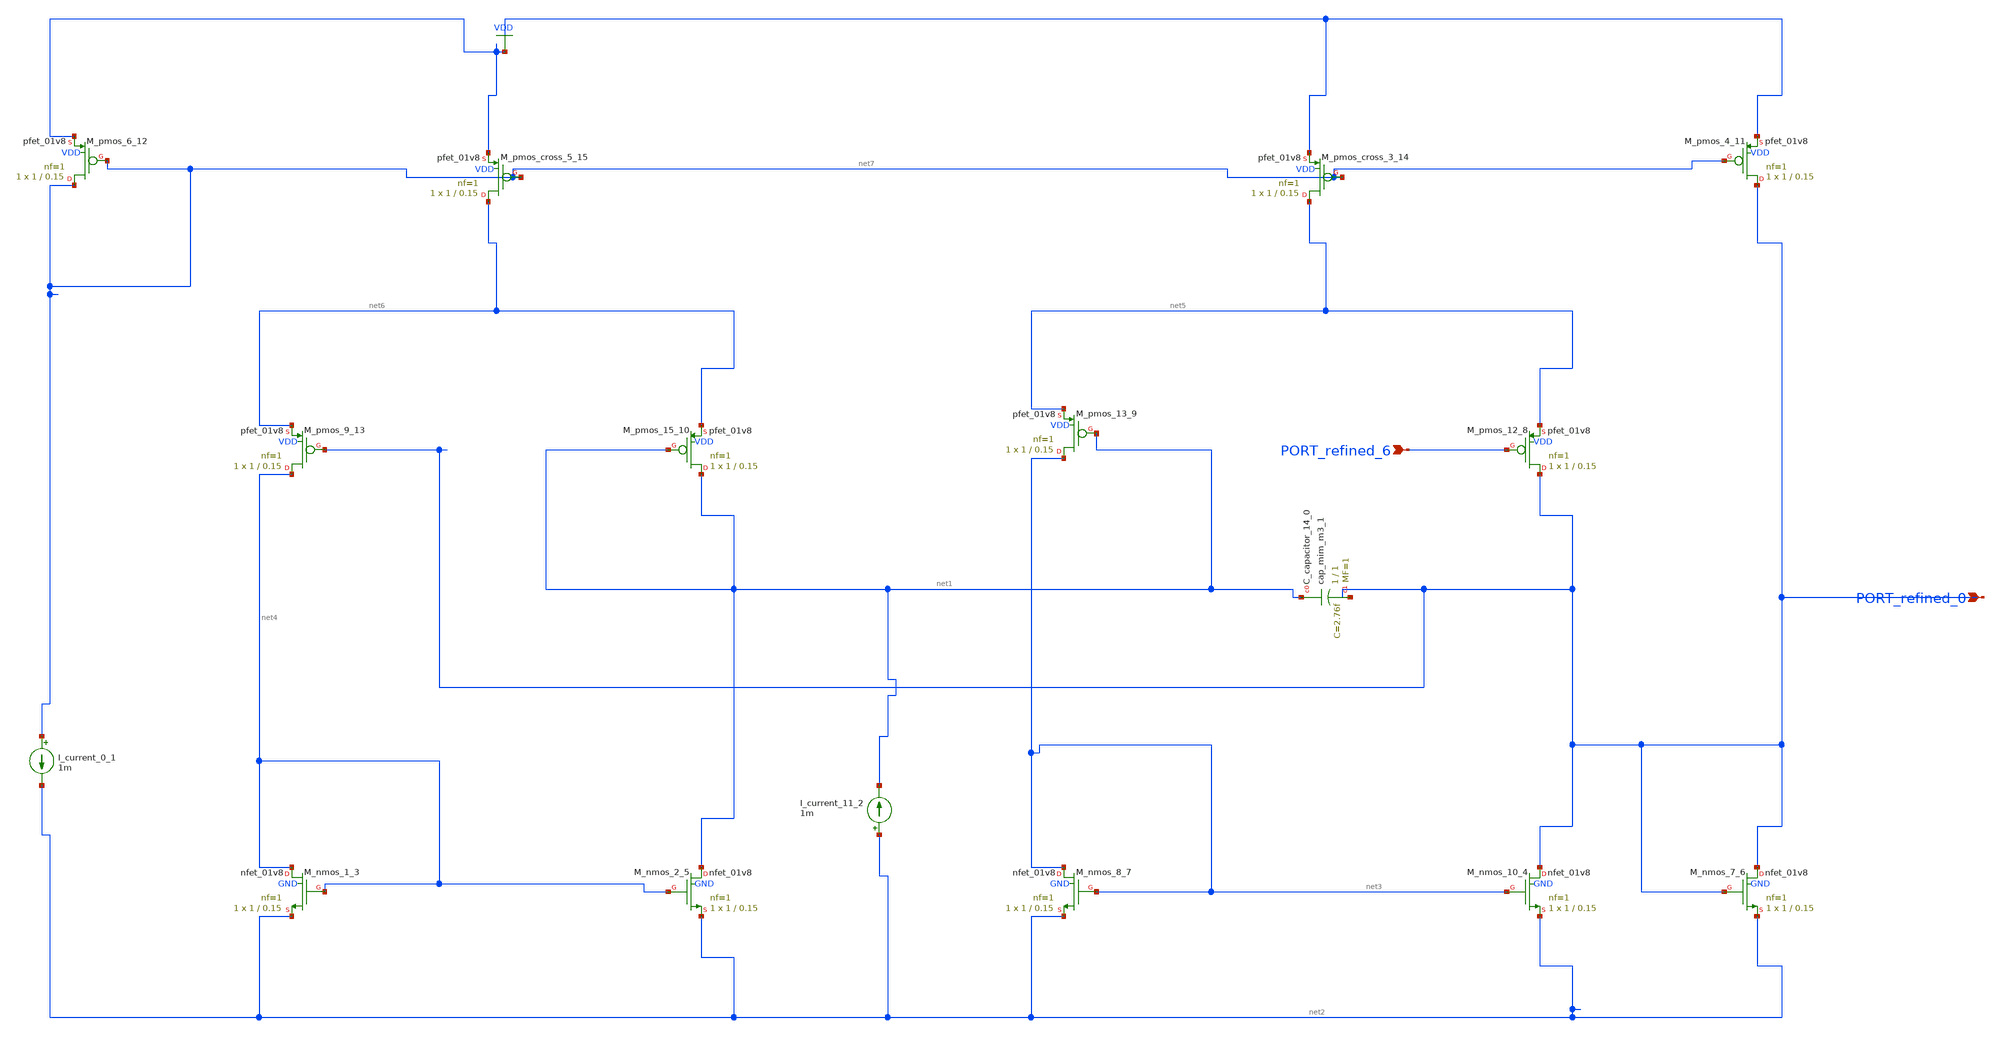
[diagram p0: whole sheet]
** sch_path: schematics/10_1016_j_vlsi_2023_02_005_06_002.sch
**.subckt 10_1016_j_vlsi_2023_02_005_06_002 PORT_refined_0 PORT_refined_6
*.ipin PORT_refined_0
*.ipin PORT_refined_6
XC_capacitor_14_0 net1 PORT_refined_0 sky130_fd_pr__cap_mim_m3_1 W=1 L=1 MF=1 m=1
I_current_0_1 net7 net2 1m
I_current_11_2 net2 net1 1m
XM_nmos_1_3 net4 net4 net2 GND sky130_fd_pr__nfet_01v8 L=0.15 W=1 nf=1 ad='int((1 + 1)/2) * 1 / 1 * 0.29'
+ as='int((1 + 2)/2) * 1 / 1 * 0.29' pd='2*int((1 + 1)/2) * (1 / 1 + 0.29)' ps='2*int((1 + 2)/2) * (1 / 1 + 0.29)'
+ nrd='0.29 / 1 ' nrs='0.29 / 1 ' sa=0 sb=0 sd=0 mult=1 m=1
XM_nmos_10_4 PORT_refined_0 net3 net2 GND sky130_fd_pr__nfet_01v8 L=0.15 W=1 nf=1 ad='int((1 + 1)/2) * 1 / 1 * 0.29'
+ as='int((1 + 2)/2) * 1 / 1 * 0.29' pd='2*int((1 + 1)/2) * (1 / 1 + 0.29)' ps='2*int((1 + 2)/2) * (1 / 1 + 0.29)'
+ nrd='0.29 / 1 ' nrs='0.29 / 1 ' sa=0 sb=0 sd=0 mult=1 m=1
XM_nmos_2_5 net1 net4 net2 GND sky130_fd_pr__nfet_01v8 L=0.15 W=1 nf=1 ad='int((1 + 1)/2) * 1 / 1 * 0.29'
+ as='int((1 + 2)/2) * 1 / 1 * 0.29' pd='2*int((1 + 1)/2) * (1 / 1 + 0.29)' ps='2*int((1 + 2)/2) * (1 / 1 + 0.29)'
+ nrd='0.29 / 1 ' nrs='0.29 / 1 ' sa=0 sb=0 sd=0 mult=1 m=1
XM_nmos_7_6 PORT_refined_0 PORT_refined_0 net2 GND sky130_fd_pr__nfet_01v8 L=0.15 W=1 nf=1 ad='int((1 + 1)/2) * 1 / 1 * 0.29'
+ as='int((1 + 2)/2) * 1 / 1 * 0.29' pd='2*int((1 + 1)/2) * (1 / 1 + 0.29)' ps='2*int((1 + 2)/2) * (1 / 1 + 0.29)'
+ nrd='0.29 / 1 ' nrs='0.29 / 1 ' sa=0 sb=0 sd=0 mult=1 m=1
XM_nmos_8_7 net3 net3 net2 GND sky130_fd_pr__nfet_01v8 L=0.15 W=1 nf=1 ad='int((1 + 1)/2) * 1 / 1 * 0.29'
+ as='int((1 + 2)/2) * 1 / 1 * 0.29' pd='2*int((1 + 1)/2) * (1 / 1 + 0.29)' ps='2*int((1 + 2)/2) * (1 / 1 + 0.29)'
+ nrd='0.29 / 1 ' nrs='0.29 / 1 ' sa=0 sb=0 sd=0 mult=1 m=1
XM_pmos_12_8 PORT_refined_0 PORT_refined_6 net5 VDD sky130_fd_pr__pfet_01v8 L=0.15 W=1 nf=1 ad='int((1 + 1)/2) * 1 / 1 * 0.29'
+ as='int((1 + 2)/2) * 1 / 1 * 0.29' pd='2*int((1 + 1)/2) * (1 / 1 + 0.29)' ps='2*int((1 + 2)/2) * (1 / 1 + 0.29)'
+ nrd='0.29 / 1 ' nrs='0.29 / 1 ' sa=0 sb=0 sd=0 mult=1 m=1
XM_pmos_13_9 net3 net1 net5 VDD sky130_fd_pr__pfet_01v8 L=0.15 W=1 nf=1 ad='int((1 + 1)/2) * 1 / 1 * 0.29'
+ as='int((1 + 2)/2) * 1 / 1 * 0.29' pd='2*int((1 + 1)/2) * (1 / 1 + 0.29)' ps='2*int((1 + 2)/2) * (1 / 1 + 0.29)'
+ nrd='0.29 / 1 ' nrs='0.29 / 1 ' sa=0 sb=0 sd=0 mult=1 m=1
XM_pmos_15_10 net1 net1 net6 VDD sky130_fd_pr__pfet_01v8 L=0.15 W=1 nf=1 ad='int((1 + 1)/2) * 1 / 1 * 0.29'
+ as='int((1 + 2)/2) * 1 / 1 * 0.29' pd='2*int((1 + 1)/2) * (1 / 1 + 0.29)' ps='2*int((1 + 2)/2) * (1 / 1 + 0.29)'
+ nrd='0.29 / 1 ' nrs='0.29 / 1 ' sa=0 sb=0 sd=0 mult=1 m=1
XM_pmos_4_11 PORT_refined_0 net7 VDD VDD sky130_fd_pr__pfet_01v8 L=0.15 W=1 nf=1 ad='int((1 + 1)/2) * 1 / 1 * 0.29'
+ as='int((1 + 2)/2) * 1 / 1 * 0.29' pd='2*int((1 + 1)/2) * (1 / 1 + 0.29)' ps='2*int((1 + 2)/2) * (1 / 1 + 0.29)'
+ nrd='0.29 / 1 ' nrs='0.29 / 1 ' sa=0 sb=0 sd=0 mult=1 m=1
XM_pmos_6_12 net7 net7 VDD VDD sky130_fd_pr__pfet_01v8 L=0.15 W=1 nf=1 ad='int((1 + 1)/2) * 1 / 1 * 0.29'
+ as='int((1 + 2)/2) * 1 / 1 * 0.29' pd='2*int((1 + 1)/2) * (1 / 1 + 0.29)' ps='2*int((1 + 2)/2) * (1 / 1 + 0.29)'
+ nrd='0.29 / 1 ' nrs='0.29 / 1 ' sa=0 sb=0 sd=0 mult=1 m=1
XM_pmos_9_13 net4 PORT_refined_0 net6 VDD sky130_fd_pr__pfet_01v8 L=0.15 W=1 nf=1 ad='int((1 + 1)/2) * 1 / 1 * 0.29'
+ as='int((1 + 2)/2) * 1 / 1 * 0.29' pd='2*int((1 + 1)/2) * (1 / 1 + 0.29)' ps='2*int((1 + 2)/2) * (1 / 1 + 0.29)'
+ nrd='0.29 / 1 ' nrs='0.29 / 1 ' sa=0 sb=0 sd=0 mult=1 m=1
XM_pmos_cross_3_14 net5 net7 VDD VDD sky130_fd_pr__pfet_01v8 L=0.15 W=1 nf=1 ad='int((1 + 1)/2) * 1 / 1 * 0.29'
+ as='int((1 + 2)/2) * 1 / 1 * 0.29' pd='2*int((1 + 1)/2) * (1 / 1 + 0.29)' ps='2*int((1 + 2)/2) * (1 / 1 + 0.29)'
+ nrd='0.29 / 1 ' nrs='0.29 / 1 ' sa=0 sb=0 sd=0 mult=1 m=1
XM_pmos_cross_5_15 net6 net7 VDD VDD sky130_fd_pr__pfet_01v8 L=0.15 W=1 nf=1 ad='int((1 + 1)/2) * 1 / 1 * 0.29'
+ as='int((1 + 2)/2) * 1 / 1 * 0.29' pd='2*int((1 + 1)/2) * (1 / 1 + 0.29)' ps='2*int((1 + 2)/2) * (1 / 1 + 0.29)'
+ nrd='0.29 / 1 ' nrs='0.29 / 1 ' sa=0 sb=0 sd=0 mult=1 m=1
**.ends
.GLOBAL VDD
.end
